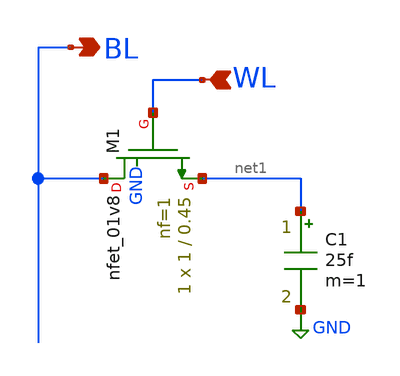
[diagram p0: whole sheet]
** sch_path: Circuiti/memories/d_RAM.sch
**.subckt d_RAM WL BL
*.ipin WL
*.opin BL
XM1 BL WL net1 GND sky130_fd_pr__nfet_01v8 L=0.45 W=1 nf=1 ad='int((nf+1)/2) * W/nf * 0.29' as='int((nf+2)/2) * W/nf * 0.29'
+ pd='2*int((nf+1)/2) * (W/nf + 0.29)' ps='2*int((nf+2)/2) * (W/nf + 0.29)' nrd='0.29 / W' nrs='0.29 / W'
+ sa=0 sb=0 sd=0 mult=1 m=1
C1 net1 GND 25f m=1
**.ends
.GLOBAL GND
.end
